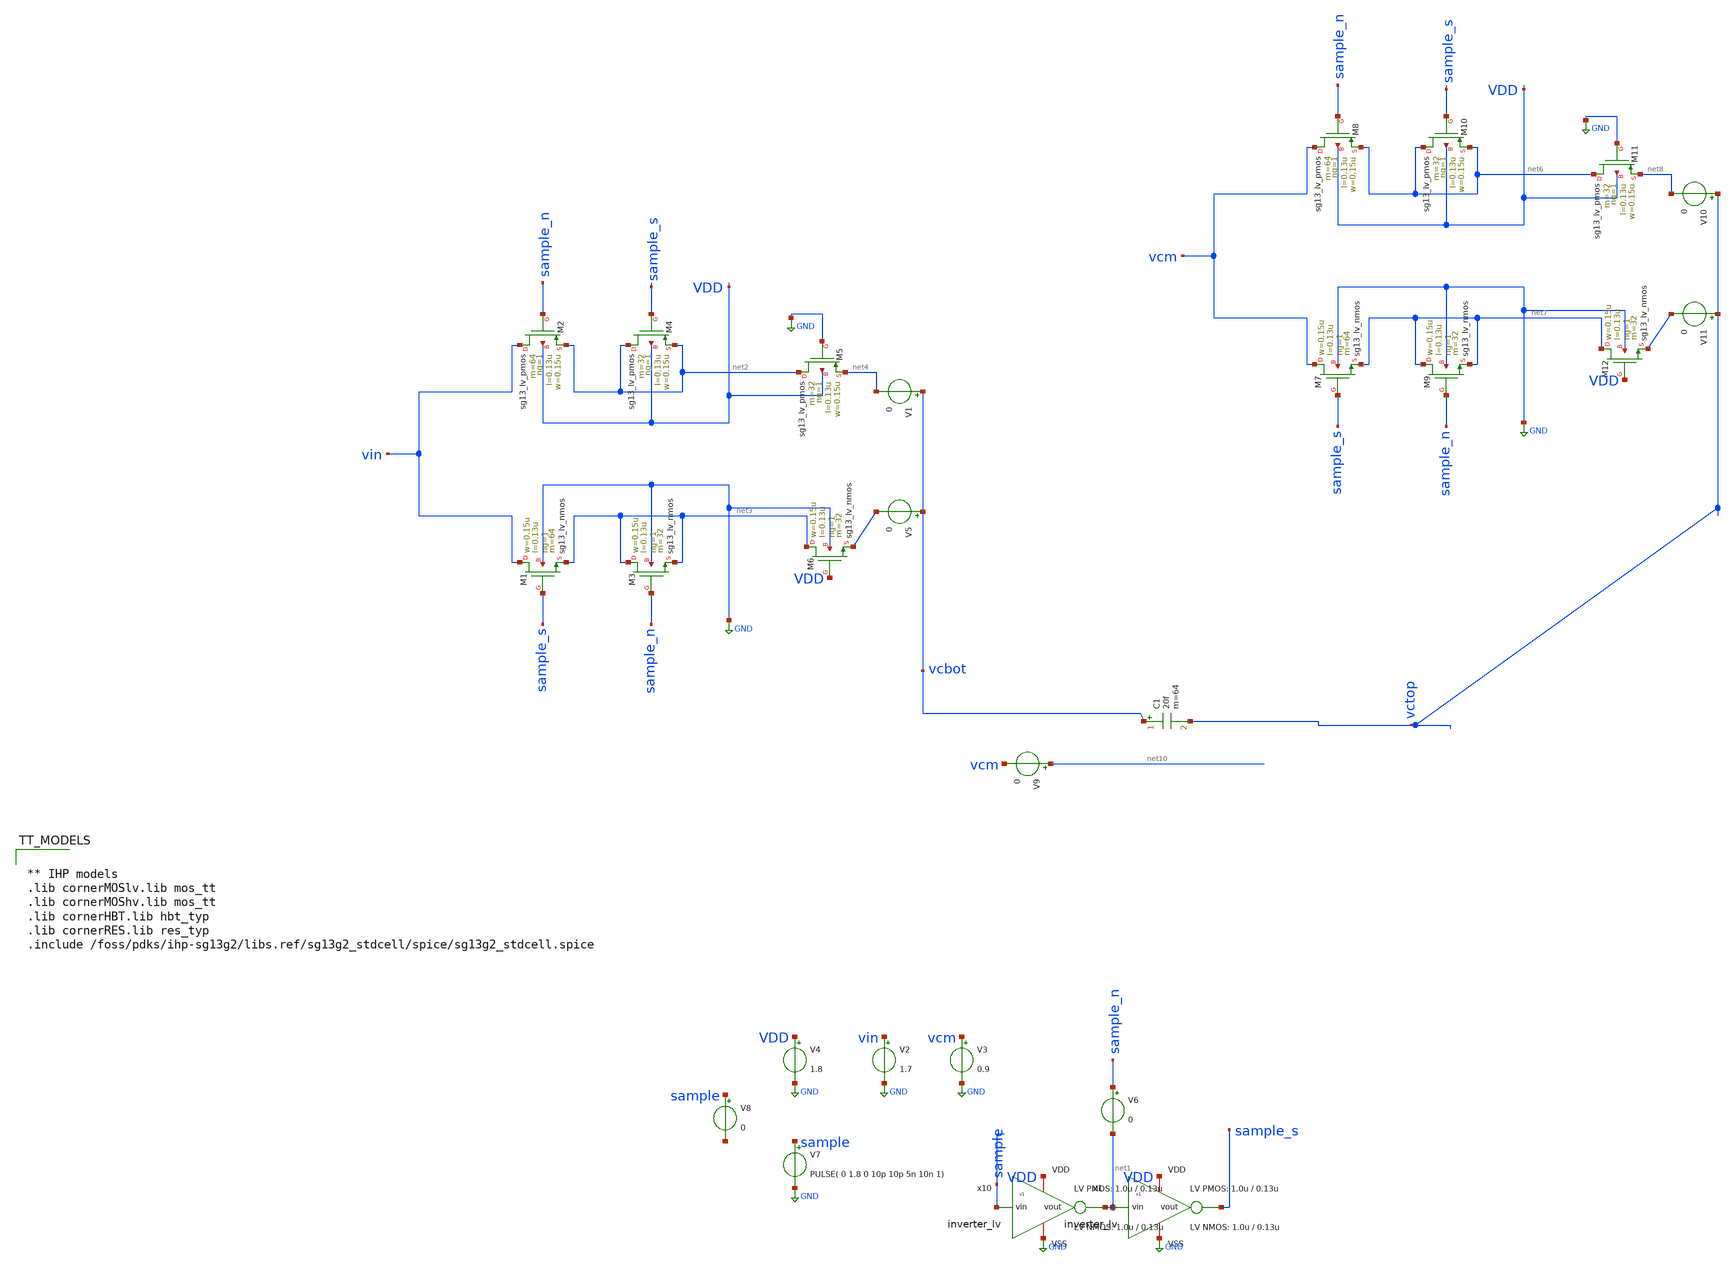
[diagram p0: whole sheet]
** sch_path: xschem/dac_icms_cell/testbenches/tb_capacitor.sch
**.subckt tb_capacitor
V7 sample GND PULSE( 0 1.8 0 10p 10p 5n 10n 1)
x10 VDD sample net1 GND inverter_lv W_P=1.0u L_P=0.13u W_N=1.0u L_N=0.13u N_C=1
V2 vin GND 1.7
V3 vcm GND 0.9
V4 VDD GND 1.8
C1 vcbot vctop 20f m=64
V1 vcbot net4 0
V5 vcbot net5 0
V6 sample_n net1 0
V8 sample net11 0
XM1 vin sample_s net3 GND sg13_lv_nmos w=0.15u l=0.13u ng=1 m=64 mm_ok=1
XM2 vin sample_n net2 VDD sg13_lv_pmos w=0.15u l=0.13u ng=1 m=64 mm_ok=1
XM3 net3 sample_n net3 GND sg13_lv_nmos w=0.15u l=0.13u ng=1 m=32 mm_ok=1
XM4 net2 sample_s net2 VDD sg13_lv_pmos w=0.15u l=0.13u ng=1 m=32 mm_ok=1
x1 VDD net1 sample_s GND inverter_lv W_P=1.0u L_P=0.13u W_N=1.0u L_N=0.13u N_C=1
V9 net10 vcm 0
XM5 net2 GND net4 VDD sg13_lv_pmos w=0.15u l=0.13u ng=1 m=32 mm_ok=1
XM6 net3 VDD net5 GND sg13_lv_nmos w=0.15u l=0.13u ng=1 m=32 mm_ok=1
V10 vctop net8 0
V11 vctop net9 0
XM7 vcm sample_s net7 GND sg13_lv_nmos w=0.15u l=0.13u ng=1 m=64 mm_ok=1
XM8 vcm sample_n net6 VDD sg13_lv_pmos w=0.15u l=0.13u ng=1 m=64 mm_ok=1
XM9 net7 sample_n net7 GND sg13_lv_nmos w=0.15u l=0.13u ng=1 m=32 mm_ok=1
XM10 net6 sample_s net6 VDD sg13_lv_pmos w=0.15u l=0.13u ng=1 m=32 mm_ok=1
XM11 net6 GND net8 VDD sg13_lv_pmos w=0.15u l=0.13u ng=1 m=32 mm_ok=1
XM12 net7 VDD net9 GND sg13_lv_nmos w=0.15u l=0.13u ng=1 m=32 mm_ok=1
**** begin user architecture code


.param temp=27
.param W_P = 1.0u
.param L_P = 0.13u
.param W_N = 1.0u
.param L_N = 0.13u
.options savecurrents klu method=gear reltol=1e-2 abstol=1e-15 gmin=1e-10
.control

* Transient Analysis
tran 100p 20n

*plot {d0} {d1 + 4} {d2 + 8} {d3 + 12} {d4 + 16} {d5 + 20} {d6 + 24} {d7 + 28} {d8 + 32} {d9 + 36} {d10 + 40}
*+ {d11 + 44}
*plot {b0} {b1 + 4} {b2 + 8} {b3 + 12} {b4 + 16} {b5 + 20} {b6 + 24} {b7 + 28} {b8 + 32} {b9 + 36} {b10 + 40}
*+ {b11 + 44}
*plot {clk} {comp_in + 2} {sample + 4}
plot vctop vcbot sample
plot {vctop-vcbot} sample
plot i(v1) i(v5)
*plot x3.x14.net1-vctop x3.x18.vcap-vcbot

.endc




** IHP models
.lib cornerMOSlv.lib mos_tt
.lib cornerMOShv.lib mos_tt
.lib cornerHBT.lib hbt_typ
.lib cornerRES.lib res_typ
.include /foss/pdks/ihp-sg13g2/libs.ref/sg13g2_stdcell/spice/sg13g2_stdcell.spice


**** end user architecture code
**.ends

* expanding   symbol:  inverter/inverter_lv.sym # of pins=4
** sym_path: xschem/inverter/inverter_lv.sym
** sch_path: xschem/inverter/inverter_lv.sch
.subckt inverter_lv VDD vin vout VSS  W_P=3.0u L_P=0.13u W_N=1.0u L_N=0.13u N_C=1
*.ipin vin
*.iopin VDD
*.iopin VSS
*.opin vout
XM1 vout vin VDD VDD sg13_lv_pmos w=W_P l=L_P ng=1 m={N_C} mm_ok=1
XM2 vout vin VSS VSS sg13_lv_nmos w=W_N l=L_N ng=1 m={N_C} mm_ok=1
.ends

.GLOBAL GND
.end
